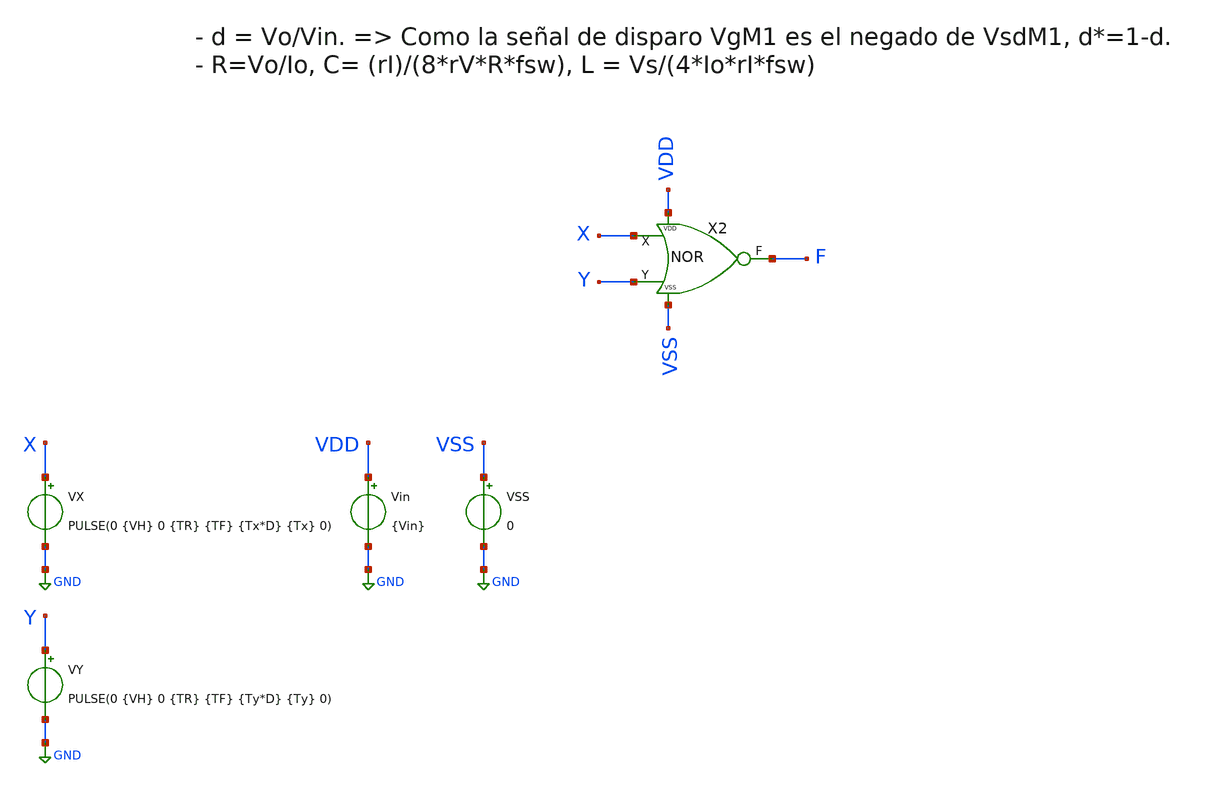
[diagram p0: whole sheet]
** sch_path: xschem/DigitalGates/TB_NOR.sch
**.subckt TB_NOR
Vin VDD GND {Vin}
VY Y GND PULSE(0 {VH} 0 {TR} {TF} {Ty*D} {Ty} 0)
VX X GND PULSE(0 {VH} 0 {TR} {TF} {Tx*D} {Tx} 0)
VSS VSS GND 0
X2 VDD VSS F X Y NOR
**** begin user architecture code


.param Vin = 1.2
.param VH = 1.2
.param Del = 0

*.param fsw = 10Meg
*.param fsw = 8.4Meg
.param fsw = 1Meg

.param Tx = 1/fsw
.param Ty = Tx/5
.param D = 0.5
.param TR = 1n
.param TF = 1n
.param TdR = 0.5n
.param TdF = 0.5n

*.option temp = 125
*.option temp = -40
.option temp = 27





.save all
.param SimTime = 5*Tx
.csparam Sim_end = {SimTime}
*.csparam T = {T}

.tran 1n {SimTime} uic

.control
run
*meas tran P_M2_mean AVG P_M2 FROM={Tmeas_i} TO={Tmeas_end}

plot v(X) v(Y)+2 v(F)+4
*write TB_DCDCBuck.raw
.endc


.end




.param temp=27
.param mult = 1

.param w_P_NOR =0.15u
.param l_P_NOR = 0.15u

.param w_N_NOR =0.15u
.param l_N_NOR =0.15u








.lib cornerMOShv.lib mos_tt
.lib cornerMOSlv.lib mos_tt
*.lib cornerMOShv.lib mos_ff
*.lib cornerMOSlv.lib mos_ff
*.lib cornerMOShv.lib mos_ss
*.lib cornerMOSlv.lib mos_ss
*.lib cornerMOShv.lib mos_sf
*.lib cornerMOSlv.lib mos_sf
*.lib cornerMOShv.lib mos_fs
*.lib cornerMOSlv.lib mos_fs

*.include /opt/pdks/ihp-sg13g2/libs.ref/sg13g2_stdcell/spice/sg13g2_stdcell.spice
*.lib $::SG13G2_MODELS/cornerRES.lib res_typ
*.lib $::SG13G2_MODELS/cornerCAP.lib cap_typ
*.lib $::SG13G2_MODELS/diodes.lib




**** end user architecture code
**.ends

* expanding   symbol:  ../DigitalGates/NOR.sym # of pins=5
** sym_path: xschem/DigitalGates/NOR.sym
** sch_path: xschem/DigitalGates/NOR.sch
.subckt NOR VDD VSS F X Y
*.iopin VDD
*.ipin X
*.opin F
*.iopin VSS
*.ipin Y
XM1 F Y VSS VSS sg13_lv_nmos w={w_N_NOR} l={l_N_NOR} ng=1 m={mult} mm_ok=1
XM2 net1 X VDD VDD sg13_lv_pmos w={w_P_NOR} l={l_P_NOR} ng=1 m={mult*3} mm_ok=1
XM4 F Y net1 VDD sg13_lv_pmos w={w_P_NOR} l={l_P_NOR} ng=1 m={mult*3} mm_ok=1
XM3 F X VSS VSS sg13_lv_nmos w={w_N_NOR} l={l_N_NOR} ng=1 m={mult} mm_ok=1
**** begin user architecture code



**** end user architecture code
.ends

.GLOBAL GND
.end
